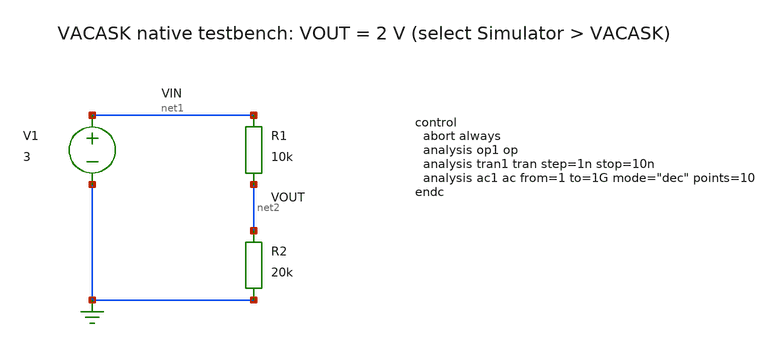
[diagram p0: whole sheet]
** sch_path: examples/vacask.sch
**.subckt vacask
R1 net1 net2 10k
R2 net2 0 20k
V1 net1 0 3
**** begin user architecture code
control
  abort always
  analysis op1 op
  analysis tran1 tran step=1n stop=10n
  analysis ac1 ac from=1 to=1G mode="dec" points=10
endc
**** end user architecture code
**.ends
.end
